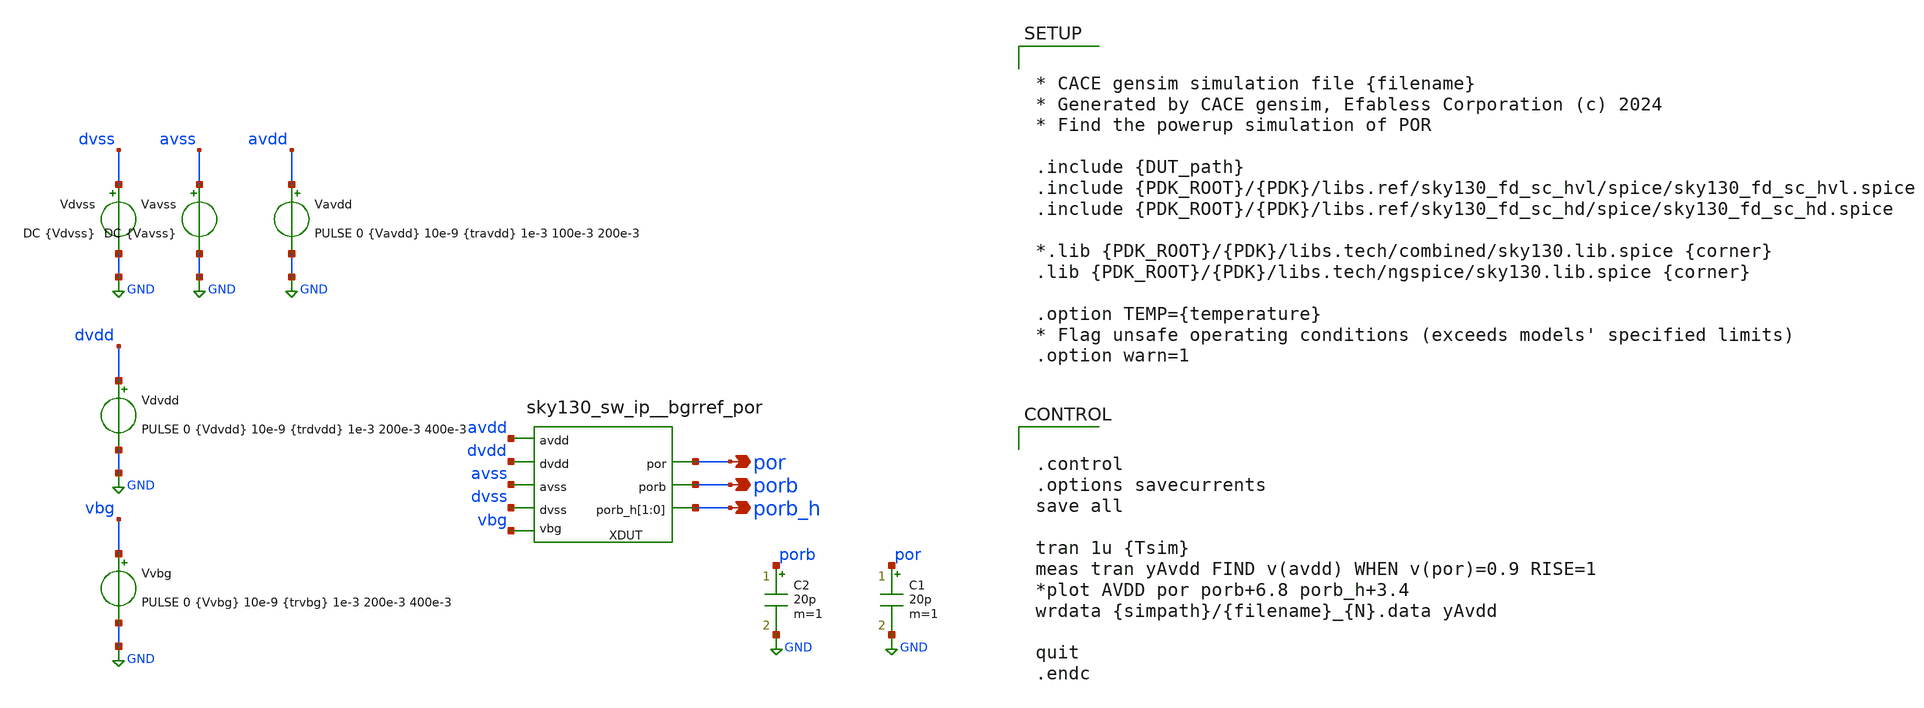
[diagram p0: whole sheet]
** sch_path: cace/rising_sim.sch
**.subckt rising_sim por porb porb_h
*.opin por
*.opin porb
*.opin porb_h
Vdvss dvss GND DC {Vdvss}
Vavdd avdd GND PULSE 0 {Vavdd} 10e-9 {travdd} 1e-3 100e-3 200e-3
Vavss avss GND DC {Vavss}
Vdvdd dvdd GND PULSE 0 {Vdvdd} 10e-9 {trdvdd} 1e-3 200e-3 400e-3
Vvbg vbg GND PULSE 0 {Vvbg} 10e-9 {trvbg} 1e-3 200e-3 400e-3
XDUT vbg por avss avdd dvdd porb dvss porb_h porb_h sky130_sw_ip__bgrref_por
C1 por GND 20p m=1
C2 porb GND 20p m=1
**** begin user architecture code


* CACE gensim simulation file {filename}
* Generated by CACE gensim, Efabless Corporation (c) 2024
* Find the powerup simulation of POR

.include {DUT_path}
.include {PDK_ROOT}/{PDK}/libs.ref/sky130_fd_sc_hvl/spice/sky130_fd_sc_hvl.spice
.include {PDK_ROOT}/{PDK}/libs.ref/sky130_fd_sc_hd/spice/sky130_fd_sc_hd.spice

*.lib {PDK_ROOT}/{PDK}/libs.tech/combined/sky130.lib.spice {corner}
.lib {PDK_ROOT}/{PDK}/libs.tech/ngspice/sky130.lib.spice {corner}

.option TEMP={temperature}
* Flag unsafe operating conditions (exceeds models' specified limits)
.option warn=1




.control
.options savecurrents
save all

tran 1u {Tsim}
meas tran yAvdd FIND v(avdd) WHEN v(por)=0.9 RISE=1
*plot AVDD por porb+6.8 porb_h+3.4
wrdata {simpath}/{filename}_{N}.data yAvdd

quit
.endc


**** end user architecture code
**.ends
.GLOBAL GND
.end
